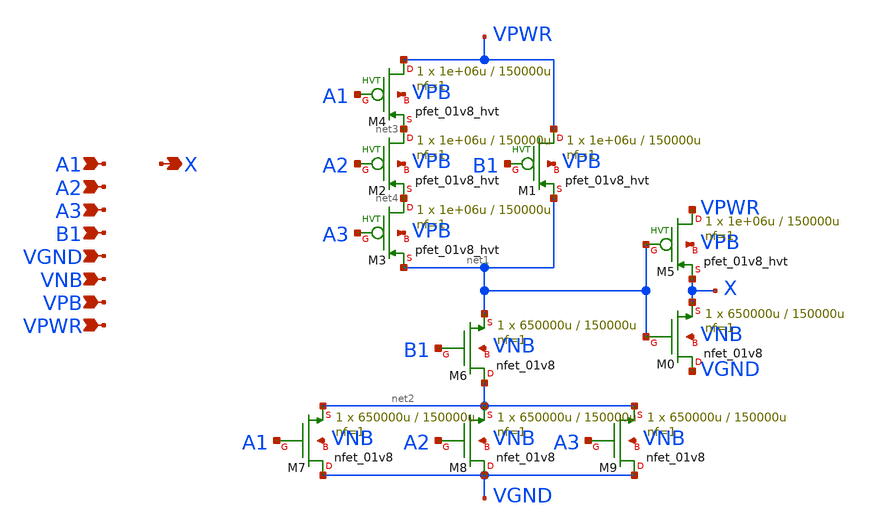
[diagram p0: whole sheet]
** sch_path: schematics/o31a/sky130_fd_sc_hd__o31a_1.sch
**.subckt sky130_fd_sc_hd__o31a_1 A1 A2 A3 B1 VGND VNB VPB VPWR X
*.ipin A1
*.ipin A2
*.ipin A3
*.ipin B1
*.ipin VGND
*.ipin VNB
*.ipin VPB
*.ipin VPWR
*.opin X
XM1 VPWR B1 net1 VPB sky130_fd_pr__pfet_01v8_hvt L=150000u W=1e+06u nf=1 ad='int((1 + 1)/2) * 1e+06u / 1 * 0.29'
+ as='int((1 + 2)/2) * 1e+06u / 1 * 0.29' pd='2*int((1 + 1)/2) * (1e+06u / 1 + 0.29)' ps='2*int((1 + 2)/2) * (1e+06u / 1 + 0.29)'
+ nrd='0.29 / 1e+06u ' nrs='0.29 / 1e+06u ' sa=0 sb=0 sd=0 mult=1 m=1
XM2 net3 A2 net4 VPB sky130_fd_pr__pfet_01v8_hvt L=150000u W=1e+06u nf=1 ad='int((1 + 1)/2) * 1e+06u / 1 * 0.29'
+ as='int((1 + 2)/2) * 1e+06u / 1 * 0.29' pd='2*int((1 + 1)/2) * (1e+06u / 1 + 0.29)' ps='2*int((1 + 2)/2) * (1e+06u / 1 + 0.29)'
+ nrd='0.29 / 1e+06u ' nrs='0.29 / 1e+06u ' sa=0 sb=0 sd=0 mult=1 m=1
XM3 net4 A3 net1 VPB sky130_fd_pr__pfet_01v8_hvt L=150000u W=1e+06u nf=1 ad='int((1 + 1)/2) * 1e+06u / 1 * 0.29'
+ as='int((1 + 2)/2) * 1e+06u / 1 * 0.29' pd='2*int((1 + 1)/2) * (1e+06u / 1 + 0.29)' ps='2*int((1 + 2)/2) * (1e+06u / 1 + 0.29)'
+ nrd='0.29 / 1e+06u ' nrs='0.29 / 1e+06u ' sa=0 sb=0 sd=0 mult=1 m=1
XM4 VPWR A1 net3 VPB sky130_fd_pr__pfet_01v8_hvt L=150000u W=1e+06u nf=1 ad='int((1 + 1)/2) * 1e+06u / 1 * 0.29'
+ as='int((1 + 2)/2) * 1e+06u / 1 * 0.29' pd='2*int((1 + 1)/2) * (1e+06u / 1 + 0.29)' ps='2*int((1 + 2)/2) * (1e+06u / 1 + 0.29)'
+ nrd='0.29 / 1e+06u ' nrs='0.29 / 1e+06u ' sa=0 sb=0 sd=0 mult=1 m=1
XM6 net2 B1 net1 VNB sky130_fd_pr__nfet_01v8 L=150000u W=650000u nf=1 ad='int((1 + 1)/2) * 650000u / 1 * 0.29'
+ as='int((1 + 2)/2) * 650000u / 1 * 0.29' pd='2*int((1 + 1)/2) * (650000u / 1 + 0.29)' ps='2*int((1 + 2)/2) * (650000u / 1 + 0.29)'
+ nrd='0.29 / 650000u ' nrs='0.29 / 650000u ' sa=0 sb=0 sd=0 mult=1 m=1
XM7 VGND A1 net2 VNB sky130_fd_pr__nfet_01v8 L=150000u W=650000u nf=1 ad='int((1 + 1)/2) * 650000u / 1 * 0.29'
+ as='int((1 + 2)/2) * 650000u / 1 * 0.29' pd='2*int((1 + 1)/2) * (650000u / 1 + 0.29)' ps='2*int((1 + 2)/2) * (650000u / 1 + 0.29)'
+ nrd='0.29 / 650000u ' nrs='0.29 / 650000u ' sa=0 sb=0 sd=0 mult=1 m=1
XM8 VGND A2 net2 VNB sky130_fd_pr__nfet_01v8 L=150000u W=650000u nf=1 ad='int((1 + 1)/2) * 650000u / 1 * 0.29'
+ as='int((1 + 2)/2) * 650000u / 1 * 0.29' pd='2*int((1 + 1)/2) * (650000u / 1 + 0.29)' ps='2*int((1 + 2)/2) * (650000u / 1 + 0.29)'
+ nrd='0.29 / 650000u ' nrs='0.29 / 650000u ' sa=0 sb=0 sd=0 mult=1 m=1
XM9 VGND A3 net2 VNB sky130_fd_pr__nfet_01v8 L=150000u W=650000u nf=1 ad='int((1 + 1)/2) * 650000u / 1 * 0.29'
+ as='int((1 + 2)/2) * 650000u / 1 * 0.29' pd='2*int((1 + 1)/2) * (650000u / 1 + 0.29)' ps='2*int((1 + 2)/2) * (650000u / 1 + 0.29)'
+ nrd='0.29 / 650000u ' nrs='0.29 / 650000u ' sa=0 sb=0 sd=0 mult=1 m=1
XM5 VPWR net1 X VPB sky130_fd_pr__pfet_01v8_hvt L=150000u W=1e+06u nf=1 ad='int((1 + 1)/2) * 1e+06u / 1 * 0.29'
+ as='int((1 + 2)/2) * 1e+06u / 1 * 0.29' pd='2*int((1 + 1)/2) * (1e+06u / 1 + 0.29)' ps='2*int((1 + 2)/2) * (1e+06u / 1 + 0.29)'
+ nrd='0.29 / 1e+06u ' nrs='0.29 / 1e+06u ' sa=0 sb=0 sd=0 mult=1 m=1
XM0 VGND net1 X VNB sky130_fd_pr__nfet_01v8 L=150000u W=650000u nf=1 ad='int((1 + 1)/2) * 650000u / 1 * 0.29'
+ as='int((1 + 2)/2) * 650000u / 1 * 0.29' pd='2*int((1 + 1)/2) * (650000u / 1 + 0.29)' ps='2*int((1 + 2)/2) * (650000u / 1 + 0.29)'
+ nrd='0.29 / 650000u ' nrs='0.29 / 650000u ' sa=0 sb=0 sd=0 mult=1 m=1
**.ends
.end
